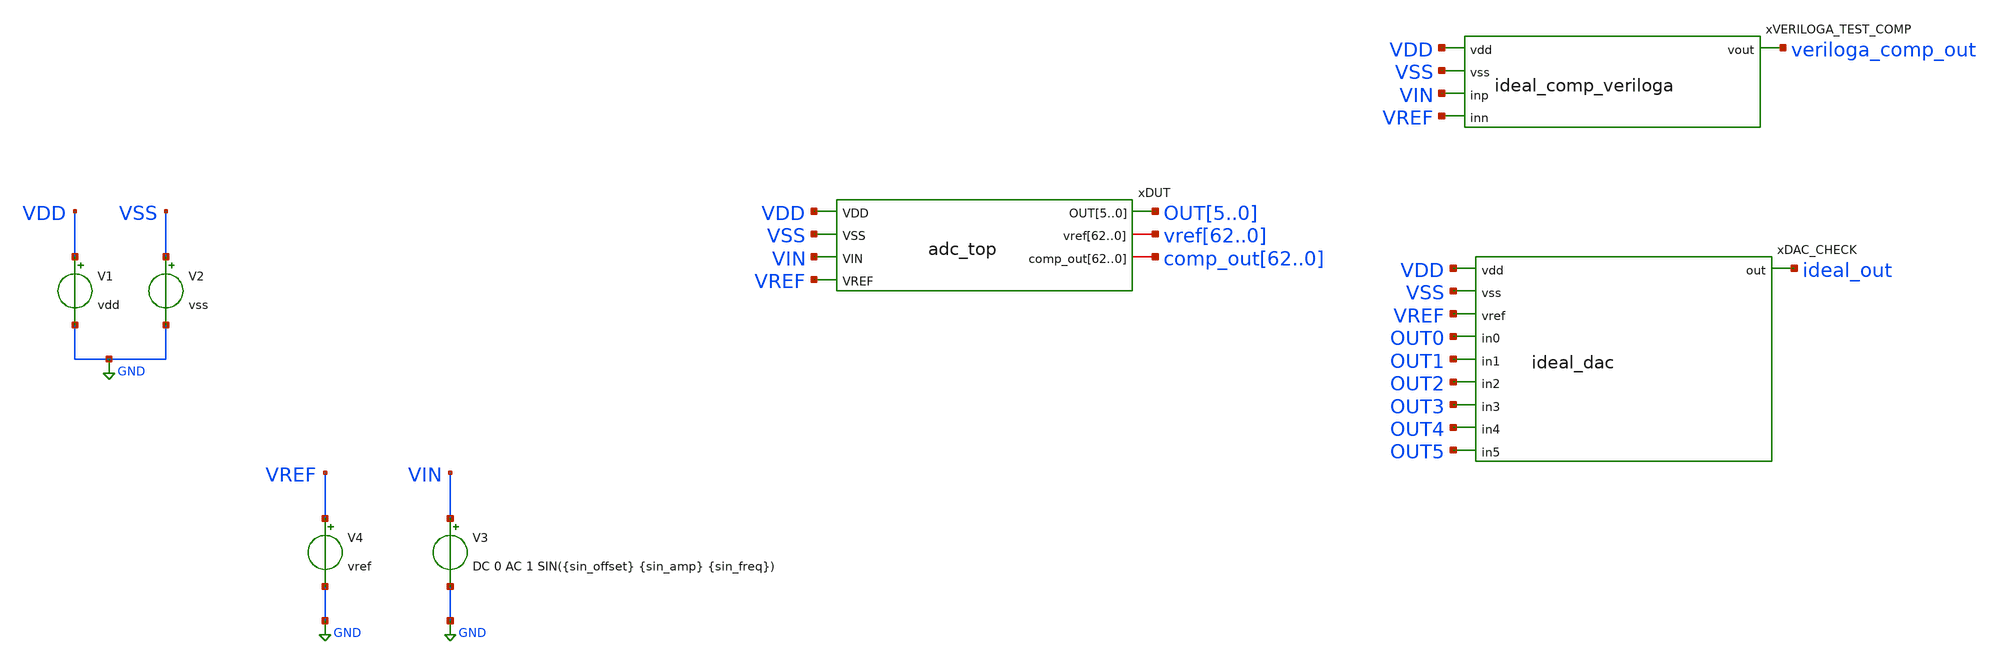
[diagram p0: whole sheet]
** sch_path: simulation/tb_adc_top.sch
**.subckt tb_adc_top
xDUT OUT5 OUT4 OUT3 OUT2 OUT1 OUT0 VDD vref62 vref61 vref60 vref59 vref58 vref57 vref56 vref55
+ vref54 vref53 vref52 vref51 vref50 vref49 vref48 vref47 vref46 vref45 vref44 vref43 vref42 vref41 vref40
+ vref39 vref38 vref37 vref36 vref35 vref34 vref33 vref32 vref31 vref30 vref29 vref28 vref27 vref26 vref25
+ vref24 vref23 vref22 vref21 vref20 vref19 vref18 vref17 vref16 vref15 vref14 vref13 vref12 vref11 vref10
+ vref9 vref8 vref7 vref6 vref5 vref4 vref3 vref2 vref1 vref0 VSS comp_out62 comp_out61 comp_out60
+ comp_out59 comp_out58 comp_out57 comp_out56 comp_out55 comp_out54 comp_out53 comp_out52 comp_out51 comp_out50
+ comp_out49 comp_out48 comp_out47 comp_out46 comp_out45 comp_out44 comp_out43 comp_out42 comp_out41 comp_out40
+ comp_out39 comp_out38 comp_out37 comp_out36 comp_out35 comp_out34 comp_out33 comp_out32 comp_out31 comp_out30
+ comp_out29 comp_out28 comp_out27 comp_out26 comp_out25 comp_out24 comp_out23 comp_out22 comp_out21 comp_out20
+ comp_out19 comp_out18 comp_out17 comp_out16 comp_out15 comp_out14 comp_out13 comp_out12 comp_out11 comp_out10
+ comp_out9 comp_out8 comp_out7 comp_out6 comp_out5 comp_out4 comp_out3 comp_out2 comp_out1 comp_out0 VIN VREF
+ adc_top
V1 VDD GND vdd
V2 VSS GND vss
V3 VIN GND DC 0 AC 1 SIN({sin_offset} {sin_amp} {sin_freq})
V4 VREF GND vref
xDAC_CHECK ideal_out VDD VSS VREF OUT0 OUT1 OUT2 OUT3 OUT4 OUT5 ideal_dac_cell
xVERILOGA_TEST_COMP VDD VSS VIN VREF veriloga_comp_out ideal_comp_cell
**** begin user architecture code



# Model files
.lib /usr/local/share/pdk/sky130A/libs.tech/ngspice/sky130.lib.spice tt
.include /usr/local/share/pdk/sky130A/libs.ref/sky130_fd_sc_hd/spice/sky130_fd_sc_hd.spice

#####################
# Global parameters #
#####################

.param vdd=1.8 vss=0 vref=vdd/2
.param sin_offset=vdd/2 sin_amp=vdd/2 sin_freq=1e6 sin_period= 1/sin_freq
.param tran_step=sin_period/1e2 tran_stop_time=sin_period*10
.param delay=sin_period*1

#####################
# Device parameters #
#####################

# Ideal comparator
.param vhigh=vdd vlow=vss

# Save nets
.save

# Run setup
.op
.tran {tran_step} {tran_stop_time} {delay}

##################
.control
##################

# Run analysis
run

let lin-tstart = 1u
let lin-stop = 99u
# let lin-tstep = 5n
linearize vin ideal_out

# Save expressions


# Write to files
write tb_adc_top.raw
wrdata ideal.txt vin ideal_out


.endc



**** end user architecture code
**.ends
.GLOBAL GND
**** begin user architecture code

.subckt ideal_dac_cell OUT VDD VSS VREF IN0 IN1 IN2 IN3 IN4 IN5
N1 out vdd vss vref in0 in1 in2 in3 in4 in5 ideal_dac_model
.ends ideal_dac_cell

.model ideal_dac_model dac_6bit


.control
* following line specifies the location for the .osdi file so ngspice can use it.
pre_osdi $working_dir/schematics/verilog_a/ideal_dac.osdi
.endc


.subckt ideal_comp_cell VDD VSS INP INN VOUT
N1 vdd vss inp inn vout ideal_comp_model
.ends ideal_comp_cell

.model ideal_comp_model ideal_comp


.control
* following line specifies the location for the .osdi file so ngspice can use it.
* working dir set in tcl in startup script as pwd in top location
pre_osdi $working_dir/schematics/verilog_a/ideal_comp.osdi
.endc

**** end user architecture code
.end
